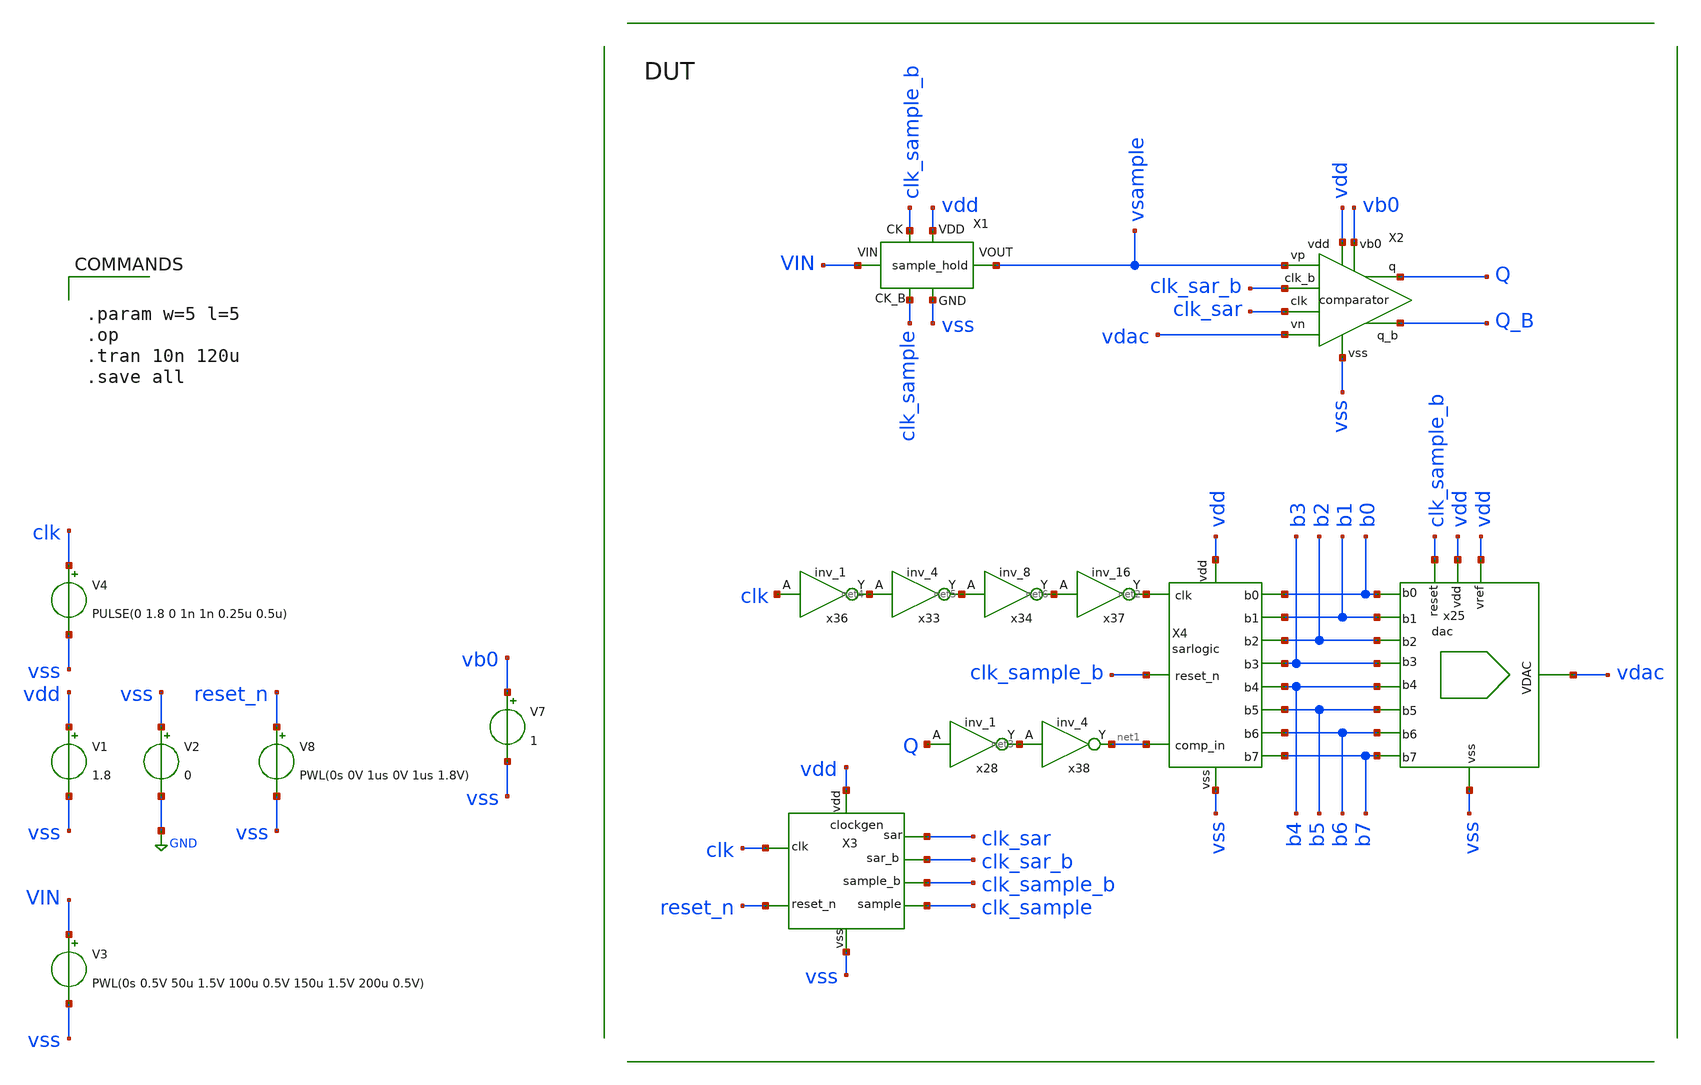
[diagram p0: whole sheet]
** sch_path: xschem/adc_top.sch
.lib $::SKYWATER_MODELS/sky130.lib.spice tt
.include $::SKYWATER_STDCELLS/sky130_fd_sc_hd.spice

**.subckt adc_top
V1 vdd vss 1.8
V3 VIN vss PWL(0s 0.5V 50u 1.5V 100u 0.5V 150u 1.5V 200u 0.5V)
V4 clk vss PULSE(0 1.8 0 1n 1n 0.25u 0.5u)
X2 vsample vdac vss Q_B Q vdd clk_sar clk_sar_b vb0 comparator
X1 vss vdd VIN vsample clk_sample_b clk_sample sample_hold
V2 vss GND 0
X4 b0 b1 net2 clk_sample_b net1 vdd vss b2 b3 b4 b5 b6 b7 sarlogic
x25 vss vdac vdd vdd b0 b1 b2 b3 b4 b5 b6 b7 clk_sample_b dac
X3 clk vdd clk_sar clk_sample vss clk_sar_b clk_sample_b reset_n clockgen
V8 reset_n vss PWL(0s 0V 1us 0V 1us 1.8V)
x28 Q vss vss vdd vdd net3 sky130_fd_sc_hd__inv_1
x36 clk vss vss vdd vdd net4 sky130_fd_sc_hd__inv_1
x38 net3 vss vss vdd vdd net1 sky130_fd_sc_hd__inv_4
x33 net4 vss vss vdd vdd net5 sky130_fd_sc_hd__inv_4
x34 net5 vss vss vdd vdd net6 sky130_fd_sc_hd__inv_8
x37 net6 vss vss vdd vdd net2 sky130_fd_sc_hd__inv_16
V7 vb0 vss 1
**** begin user architecture code


.param w=5 l=5
.op
.tran 10n 120u
.save all


**** end user architecture code
**.ends

* expanding   symbol:  xschem/comparator/comparator.sym # of pins=9
** sym_path: xschem/comparator/comparator.sym
** sch_path: xschem/comparator/comparator.sch
.subckt comparator vp vn vss q_b q vdd clk clk_b vb0
*.ipin vp
*.ipin vn
*.iopin vdd
*.ipin clk
*.iopin vss
*.opin q
*.opin q_b
*.ipin clk_b
*.ipin vb0
XM5 q_b q_comp vss vss sky130_fd_pr__nfet_01v8 L=0.15 W=0.5 nf=1 ad='int((1 + 1)/2) * 0.5 / 1 * 0.29'
+ as='int((1 + 2)/2) * 0.5 / 1 * 0.29' pd='2*int((1 + 1)/2) * (0.5 / 1 + 0.29)' ps='2*int((1 + 2)/2) * (0.5 / 1 + 0.29)'
+ nrd='0.29 / 0.5 ' nrs='0.29 / 0.5 ' sa=0 sb=0 sd=0 mult=1 m=1
XM1 q q_b_comp vss vss sky130_fd_pr__nfet_01v8 L=0.15 W=0.5 nf=1 ad='int((1 + 1)/2) * 0.5 / 1 * 0.29'
+ as='int((1 + 2)/2) * 0.5 / 1 * 0.29' pd='2*int((1 + 1)/2) * (0.5 / 1 + 0.29)' ps='2*int((1 + 2)/2) * (0.5 / 1 + 0.29)'
+ nrd='0.29 / 0.5 ' nrs='0.29 / 0.5 ' sa=0 sb=0 sd=0 mult=1 m=1
x5 q_b vss vss vdd vdd q sky130_fd_sc_hd__inv_1
x7 q vss vss vdd vdd q_b sky130_fd_sc_hd__inv_1
XM6 net1 net1 vdd vdd sky130_fd_pr__pfet_01v8 L=0.15 W=1 nf=1 ad='int((nf+1)/2) * W/nf * 0.29' as='int((nf+2)/2) * W/nf * 0.29'
+ pd='2*int((nf+1)/2) * (W/nf + 0.29)' ps='2*int((nf+2)/2) * (W/nf + 0.29)' nrd='0.29 / W' nrs='0.29 / W'
+ sa=0 sb=0 sd=0 mult=1 m=1
XM7 net1 net2 vdd vdd sky130_fd_pr__pfet_01v8 L=0.15 W=1 nf=1 ad='int((nf+1)/2) * W/nf * 0.29' as='int((nf+2)/2) * W/nf * 0.29'
+ pd='2*int((nf+1)/2) * (W/nf + 0.29)' ps='2*int((nf+2)/2) * (W/nf + 0.29)' nrd='0.29 / W' nrs='0.29 / W'
+ sa=0 sb=0 sd=0 mult=1 m=1
XM3 net2 net1 vdd vdd sky130_fd_pr__pfet_01v8 L=0.15 W=1 nf=1 ad='int((nf+1)/2) * W/nf * 0.29' as='int((nf+2)/2) * W/nf * 0.29'
+ pd='2*int((nf+1)/2) * (W/nf + 0.29)' ps='2*int((nf+2)/2) * (W/nf + 0.29)' nrd='0.29 / W' nrs='0.29 / W'
+ sa=0 sb=0 sd=0 mult=1 m=1
XM4 net2 net2 vdd vdd sky130_fd_pr__pfet_01v8 L=0.15 W=1 nf=1 ad='int((nf+1)/2) * W/nf * 0.29' as='int((nf+2)/2) * W/nf * 0.29'
+ pd='2*int((nf+1)/2) * (W/nf + 0.29)' ps='2*int((nf+2)/2) * (W/nf + 0.29)' nrd='0.29 / W' nrs='0.29 / W'
+ sa=0 sb=0 sd=0 mult=1 m=1
XM8 net2 vn net3 vss sky130_fd_pr__nfet_01v8 L=0.15 W=1 nf=1 ad='int((1 + 1)/2) * 1 / 1 * 0.29' as='int((1 + 2)/2) * 1 / 1 * 0.29'
+ pd='2*int((1 + 1)/2) * (1 / 1 + 0.29)' ps='2*int((1 + 2)/2) * (1 / 1 + 0.29)' nrd='0.29 / 1 ' nrs='0.29 / 1 '
+ sa=0 sb=0 sd=0 mult=1 m=1
XM10 net1 net1 net2 vss sky130_fd_pr__nfet_01v8 L=0.15 W=1 nf=1 ad='int((1 + 1)/2) * 1 / 1 * 0.29' as='int((1 + 2)/2) * 1 / 1 * 0.29'
+ pd='2*int((1 + 1)/2) * (1 / 1 + 0.29)' ps='2*int((1 + 2)/2) * (1 / 1 + 0.29)' nrd='0.29 / 1 ' nrs='0.29 / 1 '
+ sa=0 sb=0 sd=0 mult=1 m=1
XM11 net1 vp net3 vss sky130_fd_pr__nfet_01v8 L=0.15 W=1 nf=1 ad='int((1 + 1)/2) * 1 / 1 * 0.29' as='int((1 + 2)/2) * 1 / 1 * 0.29'
+ pd='2*int((1 + 1)/2) * (1 / 1 + 0.29)' ps='2*int((1 + 2)/2) * (1 / 1 + 0.29)' nrd='0.29 / 1 ' nrs='0.29 / 1 '
+ sa=0 sb=0 sd=0 mult=1 m=1
XM12 net2 net2 net1 vss sky130_fd_pr__nfet_01v8 L=0.15 W=1 nf=1 ad='int((1 + 1)/2) * 1 / 1 * 0.29' as='int((1 + 2)/2) * 1 / 1 * 0.29'
+ pd='2*int((1 + 1)/2) * (1 / 1 + 0.29)' ps='2*int((1 + 2)/2) * (1 / 1 + 0.29)' nrd='0.29 / 1 ' nrs='0.29 / 1 '
+ sa=0 sb=0 sd=0 mult=1 m=1
XM13 net3 vb0 vss vss sky130_fd_pr__nfet_01v8 L=1 W=2 nf=1 ad='int((1 + 1)/2) * 2 / 1 * 0.29' as='int((1 + 2)/2) * 2 / 1 * 0.29'
+ pd='2*int((1 + 1)/2) * (2 / 1 + 0.29)' ps='2*int((1 + 2)/2) * (2 / 1 + 0.29)' nrd='0.29 / 2 ' nrs='0.29 / 2 '
+ sa=0 sb=0 sd=0 mult=1 m=1
x3 vop_comp vss vss vdd vdd q_comp sky130_fd_sc_hd__inv_1
x4 von_comp vss vss vdd vdd q_b_comp sky130_fd_sc_hd__inv_1
XM2 vop vop vdd vdd sky130_fd_pr__pfet_01v8 L=0.15 W=1 nf=1 ad='int((nf+1)/2) * W/nf * 0.29' as='int((nf+2)/2) * W/nf * 0.29'
+ pd='2*int((nf+1)/2) * (W/nf + 0.29)' ps='2*int((nf+2)/2) * (W/nf + 0.29)' nrd='0.29 / W' nrs='0.29 / W'
+ sa=0 sb=0 sd=0 mult=1 m=1
XM9 vop von vdd vdd sky130_fd_pr__pfet_01v8 L=0.15 W=1 nf=1 ad='int((nf+1)/2) * W/nf * 0.29' as='int((nf+2)/2) * W/nf * 0.29'
+ pd='2*int((nf+1)/2) * (W/nf + 0.29)' ps='2*int((nf+2)/2) * (W/nf + 0.29)' nrd='0.29 / W' nrs='0.29 / W'
+ sa=0 sb=0 sd=0 mult=1 m=1
XM14 von vop vdd vdd sky130_fd_pr__pfet_01v8 L=0.15 W=1 nf=1 ad='int((nf+1)/2) * W/nf * 0.29' as='int((nf+2)/2) * W/nf * 0.29'
+ pd='2*int((nf+1)/2) * (W/nf + 0.29)' ps='2*int((nf+2)/2) * (W/nf + 0.29)' nrd='0.29 / W' nrs='0.29 / W'
+ sa=0 sb=0 sd=0 mult=1 m=1
XM15 von von vdd vdd sky130_fd_pr__pfet_01v8 L=0.15 W=1 nf=1 ad='int((nf+1)/2) * W/nf * 0.29' as='int((nf+2)/2) * W/nf * 0.29'
+ pd='2*int((nf+1)/2) * (W/nf + 0.29)' ps='2*int((nf+2)/2) * (W/nf + 0.29)' nrd='0.29 / W' nrs='0.29 / W'
+ sa=0 sb=0 sd=0 mult=1 m=1
XM16 von net2 net4 vss sky130_fd_pr__nfet_01v8 L=0.15 W=1 nf=1 ad='int((1 + 1)/2) * 1 / 1 * 0.29' as='int((1 + 2)/2) * 1 / 1 * 0.29'
+ pd='2*int((1 + 1)/2) * (1 / 1 + 0.29)' ps='2*int((1 + 2)/2) * (1 / 1 + 0.29)' nrd='0.29 / 1 ' nrs='0.29 / 1 '
+ sa=0 sb=0 sd=0 mult=1 m=1
XM17 vop vop von vss sky130_fd_pr__nfet_01v8 L=0.15 W=1 nf=1 ad='int((1 + 1)/2) * 1 / 1 * 0.29' as='int((1 + 2)/2) * 1 / 1 * 0.29'
+ pd='2*int((1 + 1)/2) * (1 / 1 + 0.29)' ps='2*int((1 + 2)/2) * (1 / 1 + 0.29)' nrd='0.29 / 1 ' nrs='0.29 / 1 '
+ sa=0 sb=0 sd=0 mult=1 m=1
XM18 vop net1 net4 vss sky130_fd_pr__nfet_01v8 L=0.15 W=1 nf=1 ad='int((1 + 1)/2) * 1 / 1 * 0.29' as='int((1 + 2)/2) * 1 / 1 * 0.29'
+ pd='2*int((1 + 1)/2) * (1 / 1 + 0.29)' ps='2*int((1 + 2)/2) * (1 / 1 + 0.29)' nrd='0.29 / 1 ' nrs='0.29 / 1 '
+ sa=0 sb=0 sd=0 mult=1 m=1
XM19 von von vop vss sky130_fd_pr__nfet_01v8 L=0.15 W=1 nf=1 ad='int((1 + 1)/2) * 1 / 1 * 0.29' as='int((1 + 2)/2) * 1 / 1 * 0.29'
+ pd='2*int((1 + 1)/2) * (1 / 1 + 0.29)' ps='2*int((1 + 2)/2) * (1 / 1 + 0.29)' nrd='0.29 / 1 ' nrs='0.29 / 1 '
+ sa=0 sb=0 sd=0 mult=1 m=1
XM20 net4 vb0 vss vss sky130_fd_pr__nfet_01v8 L=1 W=2 nf=1 ad='int((1 + 1)/2) * 2 / 1 * 0.29' as='int((1 + 2)/2) * 2 / 1 * 0.29'
+ pd='2*int((1 + 1)/2) * (2 / 1 + 0.29)' ps='2*int((1 + 2)/2) * (2 / 1 + 0.29)' nrd='0.29 / 2 ' nrs='0.29 / 2 '
+ sa=0 sb=0 sd=0 mult=1 m=1
XM21 net5 clk_b vss vss sky130_fd_pr__nfet_01v8 L=0.5 W=2 nf=1 ad='int((nf+1)/2) * W/nf * 0.29' as='int((nf+2)/2) * W/nf * 0.29'
+ pd='2*int((nf+1)/2) * (W/nf + 0.29)' ps='2*int((nf+2)/2) * (W/nf + 0.29)' nrd='0.29 / W' nrs='0.29 / W'
+ sa=0 sb=0 sd=0 mult=1 m=1
XM22 von_comp clk_b vdd vdd sky130_fd_pr__pfet_01v8 L=0.15 W=1 nf=1 ad='int((nf+1)/2) * W/nf * 0.29'
+ as='int((nf+2)/2) * W/nf * 0.29' pd='2*int((nf+1)/2) * (W/nf + 0.29)' ps='2*int((nf+2)/2) * (W/nf + 0.29)'
+ nrd='0.29 / W' nrs='0.29 / W' sa=0 sb=0 sd=0 mult=1 m=1
XM23 net6 clk_b vdd vdd sky130_fd_pr__pfet_01v8 L=0.15 W=1 nf=1 ad='int((nf+1)/2) * W/nf * 0.29' as='int((nf+2)/2) * W/nf * 0.29'
+ pd='2*int((nf+1)/2) * (W/nf + 0.29)' ps='2*int((nf+2)/2) * (W/nf + 0.29)' nrd='0.29 / W' nrs='0.29 / W'
+ sa=0 sb=0 sd=0 mult=1 m=1
XM24 net6 vop net5 vss sky130_fd_pr__nfet_01v8 L=0.15 W=2.5 nf=1 ad='int((nf+1)/2) * W/nf * 0.29' as='int((nf+2)/2) * W/nf * 0.29'
+ pd='2*int((nf+1)/2) * (W/nf + 0.29)' ps='2*int((nf+2)/2) * (W/nf + 0.29)' nrd='0.29 / W' nrs='0.29 / W'
+ sa=0 sb=0 sd=0 mult=1 m=1
XM25 von_comp vop_comp net6 vss sky130_fd_pr__nfet_01v8 L=0.15 W=2.5 nf=1 ad='int((nf+1)/2) * W/nf * 0.29'
+ as='int((nf+2)/2) * W/nf * 0.29' pd='2*int((nf+1)/2) * (W/nf + 0.29)' ps='2*int((nf+2)/2) * (W/nf + 0.29)'
+ nrd='0.29 / W' nrs='0.29 / W' sa=0 sb=0 sd=0 mult=1 m=1
XM26 vop_comp clk_b vdd vdd sky130_fd_pr__pfet_01v8 L=0.15 W=1 nf=1 ad='int((nf+1)/2) * W/nf * 0.29'
+ as='int((nf+2)/2) * W/nf * 0.29' pd='2*int((nf+1)/2) * (W/nf + 0.29)' ps='2*int((nf+2)/2) * (W/nf + 0.29)'
+ nrd='0.29 / W' nrs='0.29 / W' sa=0 sb=0 sd=0 mult=1 m=1
XM27 net7 clk_b vdd vdd sky130_fd_pr__pfet_01v8 L=0.15 W=1 nf=1 ad='int((nf+1)/2) * W/nf * 0.29' as='int((nf+2)/2) * W/nf * 0.29'
+ pd='2*int((nf+1)/2) * (W/nf + 0.29)' ps='2*int((nf+2)/2) * (W/nf + 0.29)' nrd='0.29 / W' nrs='0.29 / W'
+ sa=0 sb=0 sd=0 mult=1 m=1
XM28 net7 von net5 vss sky130_fd_pr__nfet_01v8 L=0.15 W=2.5 nf=1 ad='int((nf+1)/2) * W/nf * 0.29' as='int((nf+2)/2) * W/nf * 0.29'
+ pd='2*int((nf+1)/2) * (W/nf + 0.29)' ps='2*int((nf+2)/2) * (W/nf + 0.29)' nrd='0.29 / W' nrs='0.29 / W'
+ sa=0 sb=0 sd=0 mult=1 m=1
XM29 vop_comp von_comp net7 vss sky130_fd_pr__nfet_01v8 L=0.15 W=2.5 nf=1 ad='int((nf+1)/2) * W/nf * 0.29'
+ as='int((nf+2)/2) * W/nf * 0.29' pd='2*int((nf+1)/2) * (W/nf + 0.29)' ps='2*int((nf+2)/2) * (W/nf + 0.29)'
+ nrd='0.29 / W' nrs='0.29 / W' sa=0 sb=0 sd=0 mult=1 m=1
XM30 vop_comp von_comp vdd vdd sky130_fd_pr__pfet_01v8 L=0.15 W=2.5 nf=1 ad='int((nf+1)/2) * W/nf * 0.29'
+ as='int((nf+2)/2) * W/nf * 0.29' pd='2*int((nf+1)/2) * (W/nf + 0.29)' ps='2*int((nf+2)/2) * (W/nf + 0.29)'
+ nrd='0.29 / W' nrs='0.29 / W' sa=0 sb=0 sd=0 mult=1 m=1
XM31 von_comp vop_comp vdd vdd sky130_fd_pr__pfet_01v8 L=0.15 W=2.5 nf=1 ad='int((nf+1)/2) * W/nf * 0.29'
+ as='int((nf+2)/2) * W/nf * 0.29' pd='2*int((nf+1)/2) * (W/nf + 0.29)' ps='2*int((nf+2)/2) * (W/nf + 0.29)'
+ nrd='0.29 / W' nrs='0.29 / W' sa=0 sb=0 sd=0 mult=1 m=1
XM32 net6 clk_b vdd vdd sky130_fd_pr__pfet_01v8 L=0.15 W=1 nf=1 ad='int((nf+1)/2) * W/nf * 0.29' as='int((nf+2)/2) * W/nf * 0.29'
+ pd='2*int((nf+1)/2) * (W/nf + 0.29)' ps='2*int((nf+2)/2) * (W/nf + 0.29)' nrd='0.29 / W' nrs='0.29 / W'
+ sa=0 sb=0 sd=0 mult=1 m=1
XM33 net7 clk_b vdd vdd sky130_fd_pr__pfet_01v8 L=0.15 W=1 nf=1 ad='int((nf+1)/2) * W/nf * 0.29' as='int((nf+2)/2) * W/nf * 0.29'
+ pd='2*int((nf+1)/2) * (W/nf + 0.29)' ps='2*int((nf+2)/2) * (W/nf + 0.29)' nrd='0.29 / W' nrs='0.29 / W'
+ sa=0 sb=0 sd=0 mult=1 m=1
XM34 net7 clk_b net6 vdd sky130_fd_pr__pfet_01v8 L=0.15 W=1 nf=1 ad='int((nf+1)/2) * W/nf * 0.29' as='int((nf+2)/2) * W/nf * 0.29'
+ pd='2*int((nf+1)/2) * (W/nf + 0.29)' ps='2*int((nf+2)/2) * (W/nf + 0.29)' nrd='0.29 / W' nrs='0.29 / W'
+ sa=0 sb=0 sd=0 mult=1 m=1
.ends


* expanding   symbol:  xschem/sample/sample_hold.sym # of pins=6
** sym_path: xschem/sample/sample_hold.sym
** sch_path: xschem/sample/sample_hold.sch
.subckt sample_hold GND VDD VIN VOUT CK CK_B
*.iopin GND
*.iopin VDD
*.iopin CK
*.iopin CK_B
*.iopin VIN
*.iopin VOUT
XM4 net1 CK GND GND sky130_fd_pr__nfet_01v8 L=0.15 W=10 nf=1 ad='int((nf+1)/2) * W/nf * 0.29' as='int((nf+2)/2) * W/nf * 0.29'
+ pd='2*int((nf+1)/2) * (W/nf + 0.29)' ps='2*int((nf+2)/2) * (W/nf + 0.29)' nrd='0.29 / W' nrs='0.29 / W'
+ sa=0 sb=0 sd=0 mult=1 m=1
XM1 VOUT x VIN GND sky130_fd_pr__nfet_01v8 L=0.15 W=30 nf=1 ad='int((nf+1)/2) * W/nf * 0.29' as='int((nf+2)/2) * W/nf * 0.29'
+ pd='2*int((nf+1)/2) * (W/nf + 0.29)' ps='2*int((nf+2)/2) * (W/nf + 0.29)' nrd='0.29 / W' nrs='0.29 / W'
+ sa=0 sb=0 sd=0 mult=1 m=1
XM2 p x VDD p sky130_fd_pr__pfet_01v8 L=0.15 W=20 nf=1 ad='int((nf+1)/2) * W/nf * 0.29' as='int((nf+2)/2) * W/nf * 0.29'
+ pd='2*int((nf+1)/2) * (W/nf + 0.29)' ps='2*int((nf+2)/2) * (W/nf + 0.29)' nrd='0.29 / W' nrs='0.29 / W'
+ sa=0 sb=0 sd=0 mult=1 m=1
XM3 x net2 p p sky130_fd_pr__pfet_01v8 L=0.15 W=5 nf=1 ad='int((nf+1)/2) * W/nf * 0.29' as='int((nf+2)/2) * W/nf * 0.29'
+ pd='2*int((nf+1)/2) * (W/nf + 0.29)' ps='2*int((nf+2)/2) * (W/nf + 0.29)' nrd='0.29 / W' nrs='0.29 / W'
+ sa=0 sb=0 sd=0 mult=1 m=1
XM5 net2 CK_B VDD VDD sky130_fd_pr__pfet_01v8 L=0.15 W=2 nf=1 ad='int((nf+1)/2) * W/nf * 0.29' as='int((nf+2)/2) * W/nf * 0.29'
+ pd='2*int((nf+1)/2) * (W/nf + 0.29)' ps='2*int((nf+2)/2) * (W/nf + 0.29)' nrd='0.29 / W' nrs='0.29 / W'
+ sa=0 sb=0 sd=0 mult=1 m=1
XM6 net1 CK_B net2 GND sky130_fd_pr__nfet_01v8 L=0.15 W=1 nf=1 ad='int((nf+1)/2) * W/nf * 0.29' as='int((nf+2)/2) * W/nf * 0.29'
+ pd='2*int((nf+1)/2) * (W/nf + 0.29)' ps='2*int((nf+2)/2) * (W/nf + 0.29)' nrd='0.29 / W' nrs='0.29 / W'
+ sa=0 sb=0 sd=0 mult=1 m=1
XM7 VIN x net1 GND sky130_fd_pr__nfet_01v8 L=0.15 W=10 nf=1 ad='int((nf+1)/2) * W/nf * 0.29' as='int((nf+2)/2) * W/nf * 0.29'
+ pd='2*int((nf+1)/2) * (W/nf + 0.29)' ps='2*int((nf+2)/2) * (W/nf + 0.29)' nrd='0.29 / W' nrs='0.29 / W'
+ sa=0 sb=0 sd=0 mult=1 m=1
XM8 net2 x net1 GND sky130_fd_pr__nfet_01v8 L=0.15 W=5 nf=1 ad='int((nf+1)/2) * W/nf * 0.29' as='int((nf+2)/2) * W/nf * 0.29'
+ pd='2*int((nf+1)/2) * (W/nf + 0.29)' ps='2*int((nf+2)/2) * (W/nf + 0.29)' nrd='0.29 / W' nrs='0.29 / W'
+ sa=0 sb=0 sd=0 mult=1 m=1
XM9 x VDD net3 GND sky130_fd_pr__nfet_01v8 L=0.15 W=20 nf=1 ad='int((nf+1)/2) * W/nf * 0.29' as='int((nf+2)/2) * W/nf * 0.29'
+ pd='2*int((nf+1)/2) * (W/nf + 0.29)' ps='2*int((nf+2)/2) * (W/nf + 0.29)' nrd='0.29 / W' nrs='0.29 / W'
+ sa=0 sb=0 sd=0 mult=1 m=1
XM10 net3 CK GND GND sky130_fd_pr__nfet_01v8 L=0.15 W=20 nf=1 ad='int((nf+1)/2) * W/nf * 0.29' as='int((nf+2)/2) * W/nf * 0.29'
+ pd='2*int((nf+1)/2) * (W/nf + 0.29)' ps='2*int((nf+2)/2) * (W/nf + 0.29)' nrd='0.29 / W' nrs='0.29 / W'
+ sa=0 sb=0 sd=0 mult=1 m=1
XC9 p net1 sky130_fd_pr__cap_mim_m3_1 W=15 L=15 MF=1 m=1
XC1 VOUT GND sky130_fd_pr__cap_mim_m3_1 W=5 L=5 MF=50 m=50
.ends


* expanding   symbol:  xschem/sar_logic/sarlogic.sym # of pins=13
** sym_path: xschem/sar_logic/sarlogic.sym
** sch_path: xschem/sar_logic/sarlogic.sch
.subckt sarlogic b0 b1 clk reset_n comp_in vdd vss b2 b3 b4 b5 b6 b7
*.iopin vdd
*.iopin clk
*.iopin b7
*.iopin b6
*.iopin b5
*.iopin b4
*.iopin b3
*.iopin b2
*.iopin b1
*.iopin b0
*.iopin comp_in
*.iopin vss
*.iopin reset_n
x1 clk df7 net1 vdd vss vss vdd vdd df6 df6_b sky130_fd_sc_hd__dfbbp_1
x2 clk df6 net1 vdd vss vss vdd vdd df5 df5_b sky130_fd_sc_hd__dfbbp_1
x3 clk df5 net1 vdd vss vss vdd vdd df4 df4_b sky130_fd_sc_hd__dfbbp_1
x4 clk df4 net1 vdd vss vss vdd vdd df3 df3_b sky130_fd_sc_hd__dfbbp_1
x5 clk df3 net1 vdd vss vss vdd vdd df2 df2_b sky130_fd_sc_hd__dfbbp_1
x6 clk df2 net1 vdd vss vss vdd vdd df1 df1_b sky130_fd_sc_hd__dfbbp_1
x8 clk df1 net1 vdd vss vss vdd vdd df0 df0_b sky130_fd_sc_hd__dfbbp_1
x9 clk df0 net1 vdd vss vss vdd vdd df00 df00_b sky130_fd_sc_hd__dfbbp_1
x11 b5 comp_in net1 df6_b vss vss vdd vdd b6 net4 sky130_fd_sc_hd__dfbbp_1
x12 b4 comp_in net1 df5_b vss vss vdd vdd b5 net5 sky130_fd_sc_hd__dfbbp_1
x13 b3 comp_in net1 df4_b vss vss vdd vdd b4 net6 sky130_fd_sc_hd__dfbbp_1
x14 b2 comp_in net1 df3_b vss vss vdd vdd b3 net7 sky130_fd_sc_hd__dfbbp_1
x15 b1 comp_in net1 df2_b vss vss vdd vdd b2 net8 sky130_fd_sc_hd__dfbbp_1
x16 b0 comp_in net1 df1_b vss vss vdd vdd b1 net9 sky130_fd_sc_hd__dfbbp_1
x17 net2 comp_in net1 df0_b vss vss vdd vdd b0 net10 sky130_fd_sc_hd__dfbbp_1
x18 vss vss net1 df00_b vss vss vdd vdd net2 net11 sky130_fd_sc_hd__dfbbp_1
x19 clk vss net1 net3 vss vss vdd vdd df7 df7_b sky130_fd_sc_hd__dfbbp_1
x20 b6 comp_in net1 df7_b vss vss vdd vdd b7 net12 sky130_fd_sc_hd__dfbbp_1
x27 clk reset_n vss vss vdd vdd net1 net3 sky130_fd_sc_hd__dfxbp_2
.ends


* expanding   symbol:  xschem/dac/dac.sym # of pins=13
** sym_path: xschem/dac/dac.sym
** sch_path: xschem/dac/dac.sch
.subckt dac vss vdac vdd vref s0 s1 s2 s3 s4 s5 s6 s7 reset
*.ipin s7
*.ipin s6
*.ipin s5
*.ipin s4
*.ipin s3
*.ipin s2
*.ipin s1
*.ipin s0
*.iopin vdd
*.iopin vss
*.iopin vref
*.opin vdac
*.ipin reset
XC2 net1 net2 sky130_fd_pr__cap_mim_m3_1 W=w L=l MF=8 m=8
X2 net2 vref vss vdd net14 vss dac_sw
XC1 net1 net3 sky130_fd_pr__cap_mim_m3_1 W=w L=l MF=4 m=4
X3 net3 vref vss vdd net15 vss dac_sw
X4 net4 vref vss vdd net16 vss dac_sw
X5 net5 vref vss vdd net17 vss dac_sw
XC3 net1 net4 sky130_fd_pr__cap_mim_m3_1 W=w L=l MF=2 m=2
XC4 net1 net5 sky130_fd_pr__cap_mim_m3_1 W=w L=l MF=1 m=1
XC5 vss net1 sky130_fd_pr__cap_mim_m3_1 W=w L=l MF=1 m=1
X1 net6 vref vss vdd net13 vss dac_sw
X6 net7 vref vss vdd net12 vss dac_sw
X7 net8 vref vss vdd net11 vss dac_sw
X8 net9 vref vss vdd net10 vss dac_sw
x9 vss s7 reset vss vss vdd vdd net10 sky130_fd_sc_hd__mux2_1
x10 vss s6 reset vss vss vdd vdd net11 sky130_fd_sc_hd__mux2_1
x11 vss s5 reset vss vss vdd vdd net12 sky130_fd_sc_hd__mux2_1
x12 vss s4 reset vss vss vdd vdd net13 sky130_fd_sc_hd__mux2_1
x13 vss s3 reset vss vss vdd vdd net14 sky130_fd_sc_hd__mux2_1
x14 vss s2 reset vss vss vdd vdd net15 sky130_fd_sc_hd__mux2_1
x15 vss s1 reset vss vss vdd vdd net16 sky130_fd_sc_hd__mux2_1
x16 vss s0 reset vss vss vdd vdd net17 sky130_fd_sc_hd__mux2_1
XM1 vdac net18 vss vss sky130_fd_pr__nfet_01v8 L=0.15 W=5 nf=1 ad='int((nf+1)/2) * W/nf * 0.29' as='int((nf+2)/2) * W/nf * 0.29'
+ pd='2*int((nf+1)/2) * (W/nf + 0.29)' ps='2*int((nf+2)/2) * (W/nf + 0.29)' nrd='0.29 / W' nrs='0.29 / W'
+ sa=0 sb=0 sd=0 mult=1 m=1
x17 reset vss vss vdd vdd net18 sky130_fd_sc_hd__inv_1
XC10 net1 vdac sky130_fd_pr__cap_mim_m3_1 W=w L=l MF=8/7 m=8/7
XC6 vdac net9 sky130_fd_pr__cap_mim_m3_1 W=w L=l MF=8 m=8
XC7 vdac net8 sky130_fd_pr__cap_mim_m3_1 W=w L=l MF=4 m=4
XC8 vdac net7 sky130_fd_pr__cap_mim_m3_1 W=w L=l MF=2 m=2
XC9 vdac net6 sky130_fd_pr__cap_mim_m3_1 W=w L=l MF=1 m=1
.ends


* expanding   symbol:  xschem/clockgen/clockgen.sym # of pins=8
** sym_path: xschem/clockgen/clockgen.sym
** sch_path: xschem/clockgen/clockgen.sch
.subckt clockgen clk vdd clk_sar clk_sample vss clk_sar_b clk_sample_b reset_n
*.opin clk_sar
*.opin clk_sample
*.ipin clk
*.iopin vss
*.iopin vdd
*.opin clk_sar_b
*.opin clk_sample_b
*.ipin reset_n
x5 clk vss clk_sample vss vss vdd vdd clk_sar sky130_fd_sc_hd__mux2_1
x10 net2 d1 net1 d3 vss vss vdd vdd clk_sample sky130_fd_sc_hd__and4_2
x11 clk net3 rst vss vss vdd vdd d0 net3 sky130_fd_sc_hd__dfrbp_2
x12 d1 d0 vss vss vdd vdd net4 sky130_fd_sc_hd__xor2_1
x13 clk net4 rst vss vss vdd vdd d1 net14 sky130_fd_sc_hd__dfrbp_2
x26 d1 d0 vss vss vdd vdd net7 sky130_fd_sc_hd__and2_1
x28 d2 net7 vss vss vdd vdd net5 sky130_fd_sc_hd__xor2_1
x29 d2 net7 vss vss vdd vdd net15 sky130_fd_sc_hd__and2_1
x30 d3 net15 vss vss vdd vdd net6 sky130_fd_sc_hd__xor2_1
x31 clk net5 rst vss vss vdd vdd d2 net16 sky130_fd_sc_hd__dfrbp_2
x32 clk net6 rst vss vss vdd vdd d3 net17 sky130_fd_sc_hd__dfrbp_2
x33 d0 vss vss vdd vdd net2 sky130_fd_sc_hd__inv_1
x34 d2 vss vss vdd vdd net1 sky130_fd_sc_hd__inv_1
x35 d1 d3 vss vss vdd vdd net11 sky130_fd_sc_hd__and2_1
x36 clk net11 vss vss vdd vdd net8 net18 sky130_fd_sc_hd__dfxbp_2
x37 clk_sar vss vss vdd vdd clk_sar_b sky130_fd_sc_hd__inv_1
x38 clk_sample vss vss vdd vdd net9 sky130_fd_sc_hd__inv_1
x39 clk_sample vdd reset_n vss vss vdd vdd net10 net19 sky130_fd_sc_hd__dfrbp_2
x40 net12 net8 vss vss vdd vdd net13 sky130_fd_sc_hd__xor2_1
x41 reset_n vss vss vdd vdd net12 sky130_fd_sc_hd__inv_1
x42 net13 vss vss vdd vdd rst sky130_fd_sc_hd__inv_1
x43 vss net9 net10 vss vss vdd vdd clk_sample_b sky130_fd_sc_hd__mux2_1
.ends


* expanding   symbol:  xschem/dac/dac_sw.sym # of pins=6
** sym_path: xschem/dac/dac_sw.sym
** sch_path: xschem/dac/dac_sw.sch
.subckt dac_sw c b vss vdd clk a
*.iopin vdd
*.iopin vss
*.ipin clk
*.iopin c
*.iopin a
*.iopin b
XM2 c clk b vss sky130_fd_pr__nfet_01v8 L=0.15 W=10 nf=1 ad='int((nf+1)/2) * W/nf * 0.29' as='int((nf+2)/2) * W/nf * 0.29'
+ pd='2*int((nf+1)/2) * (W/nf + 0.29)' ps='2*int((nf+2)/2) * (W/nf + 0.29)' nrd='0.29 / W' nrs='0.29 / W'
+ sa=0 sb=0 sd=0 mult=1 m=1
XM5 b net1 c vdd sky130_fd_pr__pfet_01v8 L=0.15 W=20 nf=1 ad='int((nf+1)/2) * W/nf * 0.29' as='int((nf+2)/2) * W/nf * 0.29'
+ pd='2*int((nf+1)/2) * (W/nf + 0.29)' ps='2*int((nf+2)/2) * (W/nf + 0.29)' nrd='0.29 / W' nrs='0.29 / W'
+ sa=0 sb=0 sd=0 mult=1 m=1
XM6 c net1 a vss sky130_fd_pr__nfet_01v8 L=0.15 W=10 nf=1 ad='int((nf+1)/2) * W/nf * 0.29' as='int((nf+2)/2) * W/nf * 0.29'
+ pd='2*int((nf+1)/2) * (W/nf + 0.29)' ps='2*int((nf+2)/2) * (W/nf + 0.29)' nrd='0.29 / W' nrs='0.29 / W'
+ sa=0 sb=0 sd=0 mult=1 m=1
XM7 a clk c vdd sky130_fd_pr__pfet_01v8 L=0.15 W=20 nf=1 ad='int((nf+1)/2) * W/nf * 0.29' as='int((nf+2)/2) * W/nf * 0.29'
+ pd='2*int((nf+1)/2) * (W/nf + 0.29)' ps='2*int((nf+2)/2) * (W/nf + 0.29)' nrd='0.29 / W' nrs='0.29 / W'
+ sa=0 sb=0 sd=0 mult=1 m=1
x1 clk vss vss vdd vdd net1 sky130_fd_sc_hd__inv_1
.ends

.GLOBAL GND
.end
